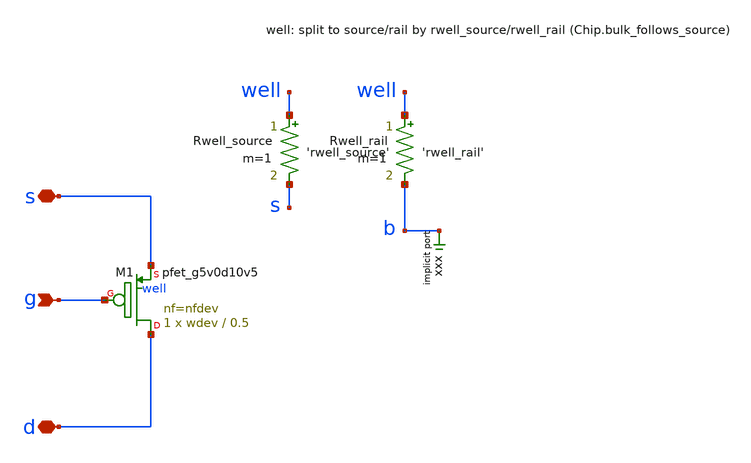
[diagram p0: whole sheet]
** sch_path: xschem/mosbius_lib/mosbius_pmos.sch
**.subckt mosbius_pmos s g d
*.iopin s
*.ipin g
*.iopin d
XM1 d g s well sky130_fd_pr__pfet_g5v0d10v5 L=0.5 W=wdev nf=nfdev ad='int((nf+1)/2) * W/nf * 0.29' as='int((nf+2)/2) * W/nf * 0.29'
+ pd='2*int((nf+1)/2) * (W/nf + 0.29)' ps='2*int((nf+2)/2) * (W/nf + 0.29)' nrd='0.29 / W' nrs='0.29 / W'
+ sa=0 sb=0 sd=0 mult=1 m=1
Rwell_source well s 'rwell_source' m=1
Rwell_rail well b 'rwell_rail' m=1
* implicit port xxx
**** begin user architecture code

.param wdev='30*w' nfdev='wdev/pmos_width_per_finger'

**** end user architecture code
**.ends
.end
